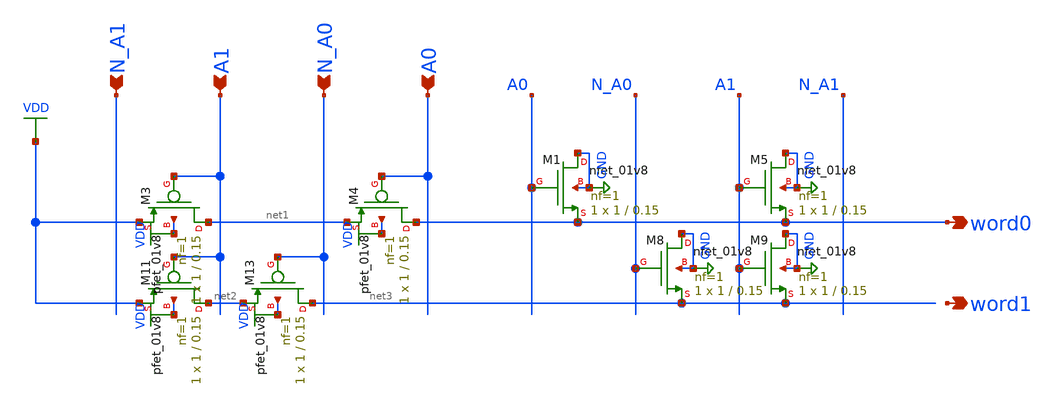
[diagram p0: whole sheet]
** sch_path: circuits/xschem/partials/decoder_test.sch
**.subckt decoder_test N_A1 A1 N_A0 A0 word0 word1
*.ipin N_A1
*.ipin A1
*.ipin N_A0
*.ipin A0
*.opin word0
*.opin word1
XM1 GND A0 word0 GND sky130_fd_pr__nfet_01v8 L=0.15 W=1 nf=1 ad='int((nf+1)/2) * W/nf * 0.29' as='int((nf+2)/2) * W/nf * 0.29'
+ pd='2*int((nf+1)/2) * (W/nf + 0.29)' ps='2*int((nf+2)/2) * (W/nf + 0.29)' nrd='0.29 / W' nrs='0.29 / W'
+ sa=0 sb=0 sd=0 mult=1 m=1
XM3 net1 A1 VDD VDD sky130_fd_pr__pfet_01v8 L=0.15 W=1 nf=1 ad='int((nf+1)/2) * W/nf * 0.29' as='int((nf+2)/2) * W/nf * 0.29'
+ pd='2*int((nf+1)/2) * (W/nf + 0.29)' ps='2*int((nf+2)/2) * (W/nf + 0.29)' nrd='0.29 / W' nrs='0.29 / W'
+ sa=0 sb=0 sd=0 mult=1 m=1
XM4 word0 A0 net1 VDD sky130_fd_pr__pfet_01v8 L=0.15 W=1 nf=1 ad='int((nf+1)/2) * W/nf * 0.29' as='int((nf+2)/2) * W/nf * 0.29'
+ pd='2*int((nf+1)/2) * (W/nf + 0.29)' ps='2*int((nf+2)/2) * (W/nf + 0.29)' nrd='0.29 / W' nrs='0.29 / W'
+ sa=0 sb=0 sd=0 mult=1 m=1
XM11 net2 A1 VDD VDD sky130_fd_pr__pfet_01v8 L=0.15 W=1 nf=1 ad='int((nf+1)/2) * W/nf * 0.29' as='int((nf+2)/2) * W/nf * 0.29'
+ pd='2*int((nf+1)/2) * (W/nf + 0.29)' ps='2*int((nf+2)/2) * (W/nf + 0.29)' nrd='0.29 / W' nrs='0.29 / W'
+ sa=0 sb=0 sd=0 mult=1 m=1
XM13 net3 N_A0 net2 VDD sky130_fd_pr__pfet_01v8 L=0.15 W=1 nf=1 ad='int((nf+1)/2) * W/nf * 0.29' as='int((nf+2)/2) * W/nf * 0.29'
+ pd='2*int((nf+1)/2) * (W/nf + 0.29)' ps='2*int((nf+2)/2) * (W/nf + 0.29)' nrd='0.29 / W' nrs='0.29 / W'
+ sa=0 sb=0 sd=0 mult=1 m=1
XM5 GND A1 word0 GND sky130_fd_pr__nfet_01v8 L=0.15 W=1 nf=1 ad='int((nf+1)/2) * W/nf * 0.29' as='int((nf+2)/2) * W/nf * 0.29'
+ pd='2*int((nf+1)/2) * (W/nf + 0.29)' ps='2*int((nf+2)/2) * (W/nf + 0.29)' nrd='0.29 / W' nrs='0.29 / W'
+ sa=0 sb=0 sd=0 mult=1 m=1
XM8 GND N_A0 net3 GND sky130_fd_pr__nfet_01v8 L=0.15 W=1 nf=1 ad='int((nf+1)/2) * W/nf * 0.29' as='int((nf+2)/2) * W/nf * 0.29'
+ pd='2*int((nf+1)/2) * (W/nf + 0.29)' ps='2*int((nf+2)/2) * (W/nf + 0.29)' nrd='0.29 / W' nrs='0.29 / W'
+ sa=0 sb=0 sd=0 mult=1 m=1
XM9 GND A1 net3 GND sky130_fd_pr__nfet_01v8 L=0.15 W=1 nf=1 ad='int((nf+1)/2) * W/nf * 0.29' as='int((nf+2)/2) * W/nf * 0.29'
+ pd='2*int((nf+1)/2) * (W/nf + 0.29)' ps='2*int((nf+2)/2) * (W/nf + 0.29)' nrd='0.29 / W' nrs='0.29 / W'
+ sa=0 sb=0 sd=0 mult=1 m=1
**.ends
.GLOBAL VDD
.GLOBAL GND
.end
